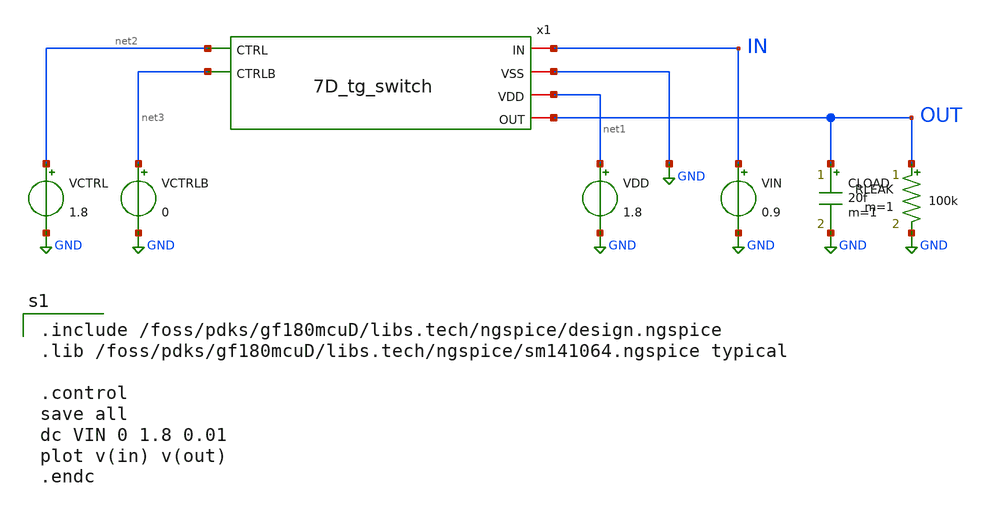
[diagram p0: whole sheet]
** sch_path: designs/libs/tb_matchmaker/tb_7D_tg_switch/tb_7D_tg_switch.sch
**.subckt tb_7D_tg_switch
x1 IN GND net1 net2 net3 OUT 7D_tg_switch
VDD net1 GND 1.8
VIN IN GND 0.9
VCTRL net2 GND 1.8
VCTRLB net3 GND 0
CLOAD OUT GND 20f m=1
RLEAK OUT GND 100k m=1
**** begin user architecture code

.include /foss/pdks/gf180mcuD/libs.tech/ngspice/design.ngspice
.lib /foss/pdks/gf180mcuD/libs.tech/ngspice/sm141064.ngspice typical

.control
save all
dc VIN 0 1.8 0.01
plot v(in) v(out)
.endc

**** end user architecture code
**.ends
.GLOBAL GND
.end
